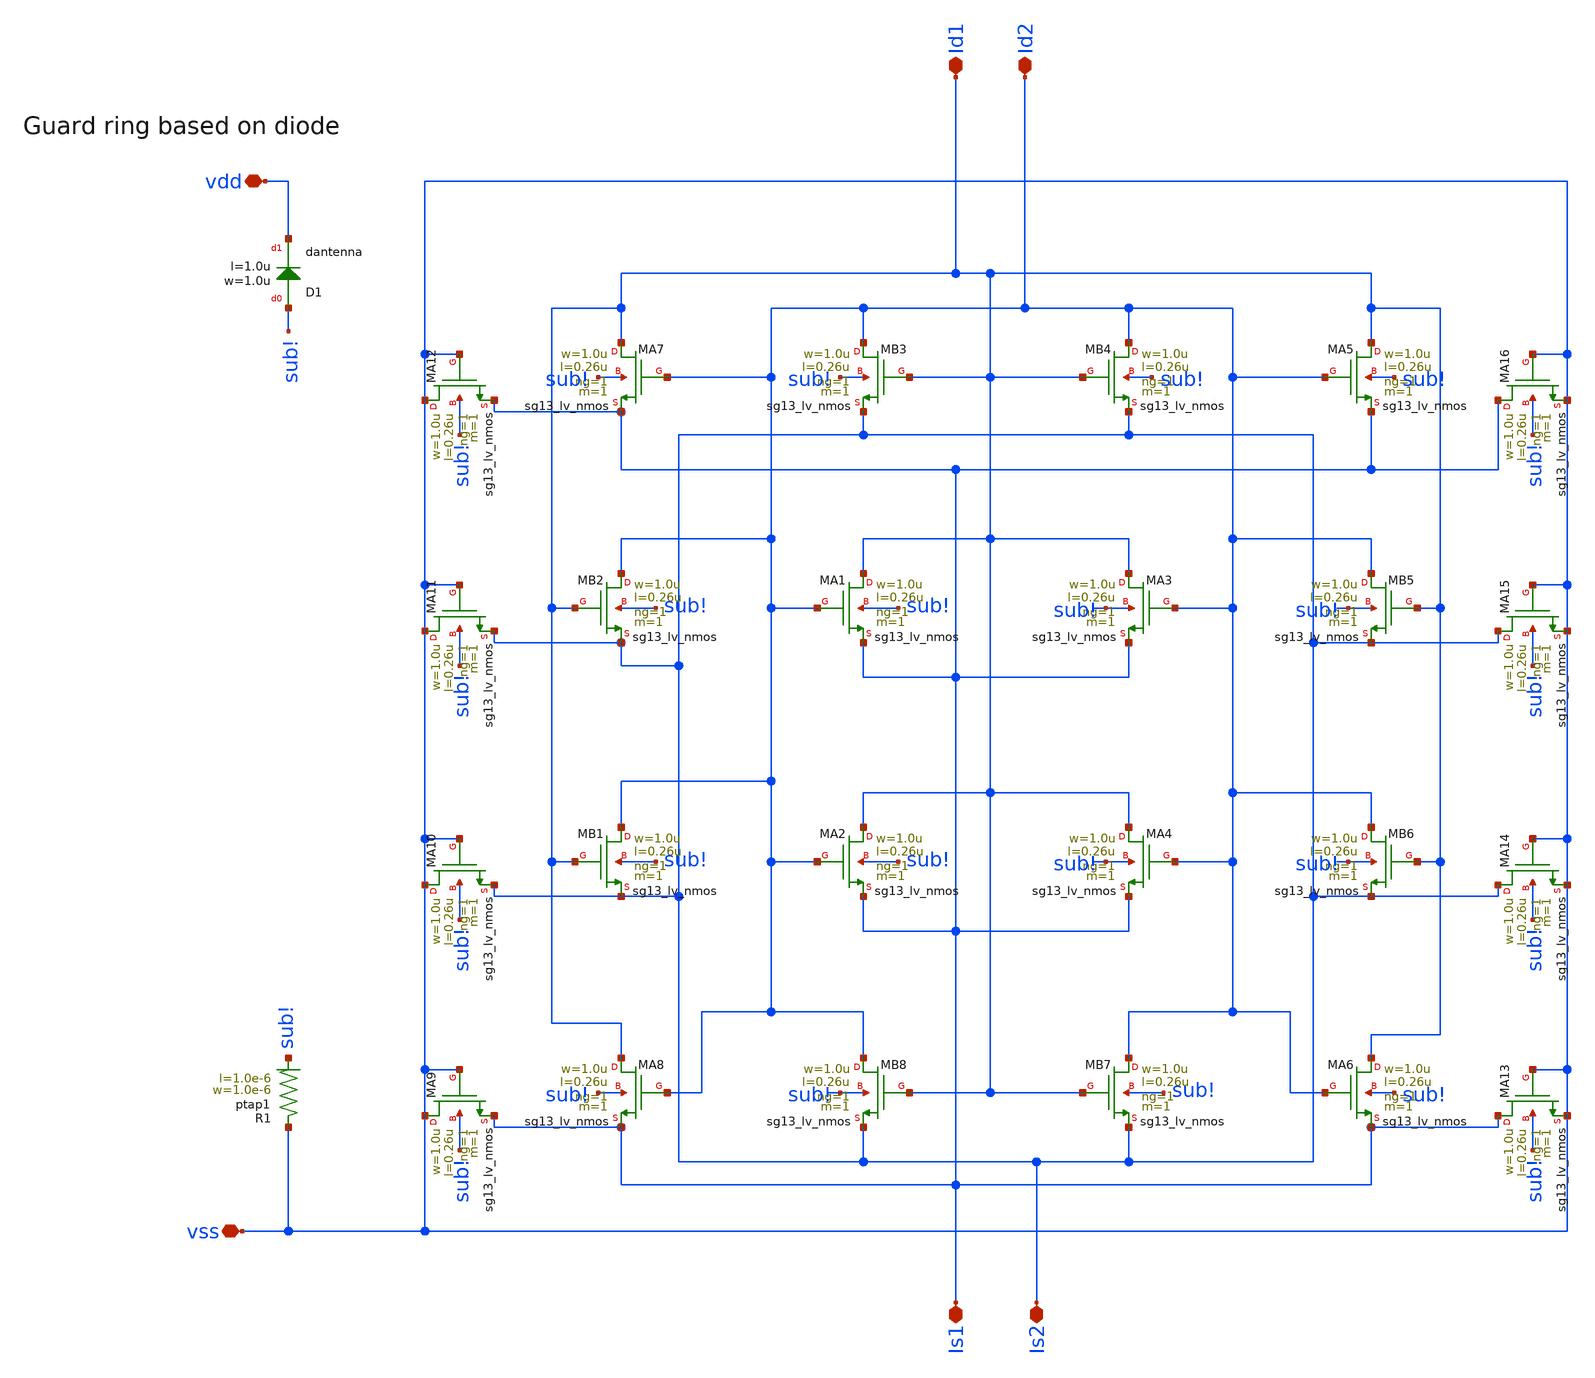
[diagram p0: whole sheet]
** sch_path: CMP7345-main/schematic/xschem/cc_pair_nmos.sch
**.subckt cc_pair_nmos vss Id2 Id1 Is2 Is1 vdd
*.iopin vss
*.iopin Id2
*.iopin Id1
*.iopin Is2
*.iopin Is1
*.iopin vdd
XMA1 Id1 Id2 Is1 sub! sg13_lv_nmos w=1.0u l=0.26u ng=1 m=1 mm_ok=0
XMA2 Id1 Id2 Is1 sub! sg13_lv_nmos w=1.0u l=0.26u ng=1 m=1 mm_ok=0
XMA3 Id1 Id2 Is1 sub! sg13_lv_nmos w=1.0u l=0.26u ng=1 m=1 mm_ok=0
XMA4 Id1 Id2 Is1 sub! sg13_lv_nmos w=1.0u l=0.26u ng=1 m=1 mm_ok=0
XMB1 Id2 Id1 Is2 sub! sg13_lv_nmos w=1.0u l=0.26u ng=1 m=1 mm_ok=0
XMB2 Id2 Id1 Is2 sub! sg13_lv_nmos w=1.0u l=0.26u ng=1 m=1 mm_ok=0
XMB3 Id2 Id1 Is2 sub! sg13_lv_nmos w=1.0u l=0.26u ng=1 m=1 mm_ok=0
XMB4 Id2 Id1 Is2 sub! sg13_lv_nmos w=1.0u l=0.26u ng=1 m=1 mm_ok=0
XMA5 Id1 Id2 Is1 sub! sg13_lv_nmos w=1.0u l=0.26u ng=1 m=1 mm_ok=0
XMA6 Id1 Id2 Is1 sub! sg13_lv_nmos w=1.0u l=0.26u ng=1 m=1 mm_ok=0
XMA7 Id1 Id2 Is1 sub! sg13_lv_nmos w=1.0u l=0.26u ng=1 m=1 mm_ok=0
XMA8 Id1 Id2 Is1 sub! sg13_lv_nmos w=1.0u l=0.26u ng=1 m=1 mm_ok=0
XMB5 Id2 Id1 Is2 sub! sg13_lv_nmos w=1.0u l=0.26u ng=1 m=1 mm_ok=0
XMB6 Id2 Id1 Is2 sub! sg13_lv_nmos w=1.0u l=0.26u ng=1 m=1 mm_ok=0
XMB7 Id2 Id1 Is2 sub! sg13_lv_nmos w=1.0u l=0.26u ng=1 m=1 mm_ok=0
XMB8 Id2 Id1 Is2 sub! sg13_lv_nmos w=1.0u l=0.26u ng=1 m=1 mm_ok=0
XMA9 vss vss Is1 sub! sg13_lv_nmos w=1.0u l=0.26u ng=1 m=1 mm_ok=0
XMA10 vss vss Is2 sub! sg13_lv_nmos w=1.0u l=0.26u ng=1 m=1 mm_ok=0
XMA11 vss vss Is2 sub! sg13_lv_nmos w=1.0u l=0.26u ng=1 m=1 mm_ok=0
XMA12 vss vss Is1 sub! sg13_lv_nmos w=1.0u l=0.26u ng=1 m=1 mm_ok=0
XMA13 Is1 vss vss sub! sg13_lv_nmos w=1.0u l=0.26u ng=1 m=1 mm_ok=0
XMA14 Is2 vss vss sub! sg13_lv_nmos w=1.0u l=0.26u ng=1 m=1 mm_ok=0
XMA15 Is2 vss vss sub! sg13_lv_nmos w=1.0u l=0.26u ng=1 m=1 mm_ok=0
XMA16 Is1 vss vss sub! sg13_lv_nmos w=1.0u l=0.26u ng=1 m=1 mm_ok=0
XD1 sub! vdd dantenna l=1.0u w=1.0u
XR1 vss sub! ptap1 R=196 w=1.0e-6 l=1.0e-6
**.ends
.end
